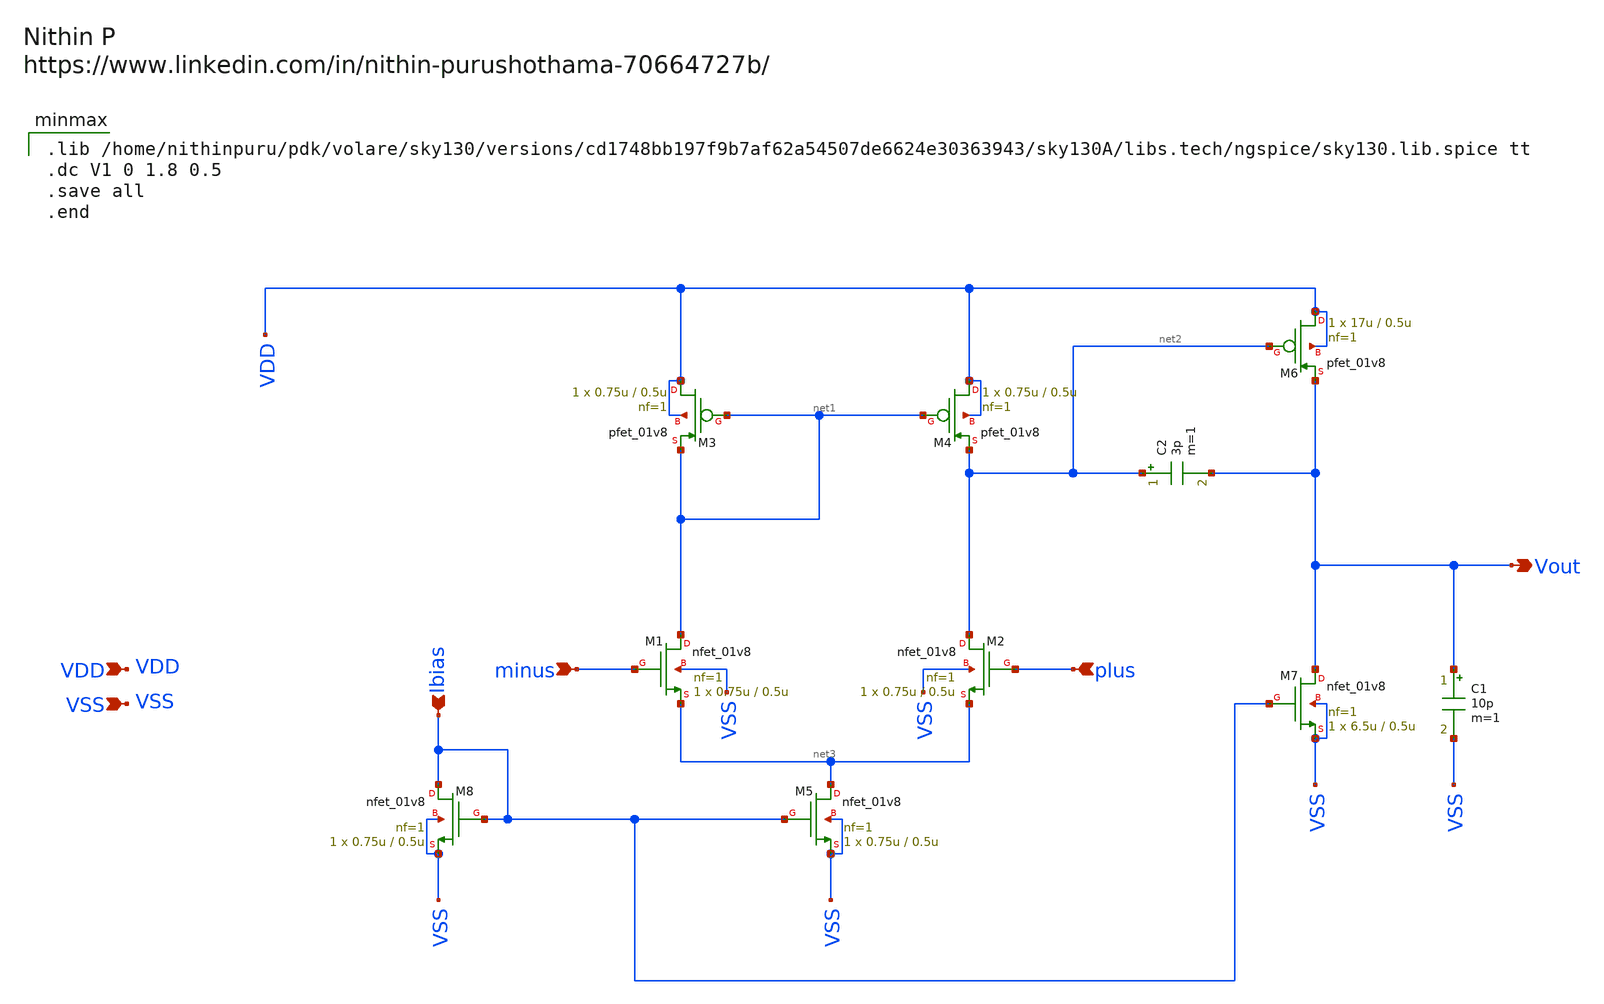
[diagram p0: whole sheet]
** sch_path: Schematics/Two stage Opamp Test bench/2stageopamp.sch
**.subckt 2stageopamp minus plus Vout VDD VSS Ibias
*.ipin minus
*.ipin plus
*.opin Vout
*.ipin VDD
*.ipin VSS
*.ipin Ibias
XM1 net1 minus net3 VSS sky130_fd_pr__nfet_01v8 L=0.5u W=0.75u nf=1 ad='int((nf+1)/2) * W/nf * 0.29'
+ as='int((nf+2)/2) * W/nf * 0.29' pd='2*int((nf+1)/2) * (W/nf + 0.29)' ps='2*int((nf+2)/2) * (W/nf + 0.29)'
+ nrd='0.29 / W' nrs='0.29 / W' sa=0 sb=0 sd=0 mult=1 m=1
XM2 net2 plus net3 VSS sky130_fd_pr__nfet_01v8 L=0.5u W=0.75u nf=1 ad='int((nf+1)/2) * W/nf * 0.29' as='int((nf+2)/2) * W/nf * 0.29'
+ pd='2*int((nf+1)/2) * (W/nf + 0.29)' ps='2*int((nf+2)/2) * (W/nf + 0.29)' nrd='0.29 / W' nrs='0.29 / W'
+ sa=0 sb=0 sd=0 mult=1 m=1
XM5 net3 Ibias VSS VSS sky130_fd_pr__nfet_01v8 L=0.5u W=0.75u nf=1 ad='int((nf+1)/2) * W/nf * 0.29' as='int((nf+2)/2) * W/nf * 0.29'
+ pd='2*int((nf+1)/2) * (W/nf + 0.29)' ps='2*int((nf+2)/2) * (W/nf + 0.29)' nrd='0.29 / W' nrs='0.29 / W'
+ sa=0 sb=0 sd=0 mult=1 m=1
XM7 Vout Ibias VSS VSS sky130_fd_pr__nfet_01v8 L=0.5u W=6.5u nf=1 ad='int((nf+1)/2) * W/nf * 0.29' as='int((nf+2)/2) * W/nf * 0.29'
+ pd='2*int((nf+1)/2) * (W/nf + 0.29)' ps='2*int((nf+2)/2) * (W/nf + 0.29)' nrd='0.29 / W' nrs='0.29 / W'
+ sa=0 sb=0 sd=0 mult=1 m=1
XM8 Ibias Ibias VSS VSS sky130_fd_pr__nfet_01v8 L=0.5u W=0.75u nf=1 ad='int((nf+1)/2) * W/nf * 0.29'
+ as='int((nf+2)/2) * W/nf * 0.29' pd='2*int((nf+1)/2) * (W/nf + 0.29)' ps='2*int((nf+2)/2) * (W/nf + 0.29)'
+ nrd='0.29 / W' nrs='0.29 / W' sa=0 sb=0 sd=0 mult=1 m=1
XM4 VDD net1 net2 VDD sky130_fd_pr__pfet_01v8 L=0.5u W=0.75u nf=1 ad='int((nf+1)/2) * W/nf * 0.29' as='int((nf+2)/2) * W/nf * 0.29'
+ pd='2*int((nf+1)/2) * (W/nf + 0.29)' ps='2*int((nf+2)/2) * (W/nf + 0.29)' nrd='0.29 / W' nrs='0.29 / W'
+ sa=0 sb=0 sd=0 mult=1 m=1
XM3 VDD net1 net1 VDD sky130_fd_pr__pfet_01v8 L=0.5u W=0.75u nf=1 ad='int((nf+1)/2) * W/nf * 0.29' as='int((nf+2)/2) * W/nf * 0.29'
+ pd='2*int((nf+1)/2) * (W/nf + 0.29)' ps='2*int((nf+2)/2) * (W/nf + 0.29)' nrd='0.29 / W' nrs='0.29 / W'
+ sa=0 sb=0 sd=0 mult=1 m=1
XM6 VDD net2 Vout VDD sky130_fd_pr__pfet_01v8 L=0.5u W=17u nf=1 ad='int((nf+1)/2) * W/nf * 0.29' as='int((nf+2)/2) * W/nf * 0.29'
+ pd='2*int((nf+1)/2) * (W/nf + 0.29)' ps='2*int((nf+2)/2) * (W/nf + 0.29)' nrd='0.29 / W' nrs='0.29 / W'
+ sa=0 sb=0 sd=0 mult=1 m=1
C2 net2 Vout 3p m=1
C1 Vout VSS 10p m=1
**** begin user architecture code

.lib /home/nithinpuru/pdk/volare/sky130/versions/cd1748bb197f9b7af62a54507de6624e30363943/sky130A/libs.tech/ngspice/sky130.lib.spice tt
.dc V1 0 1.8 0.5
.save all
.end

**** end user architecture code
**.ends
.end
